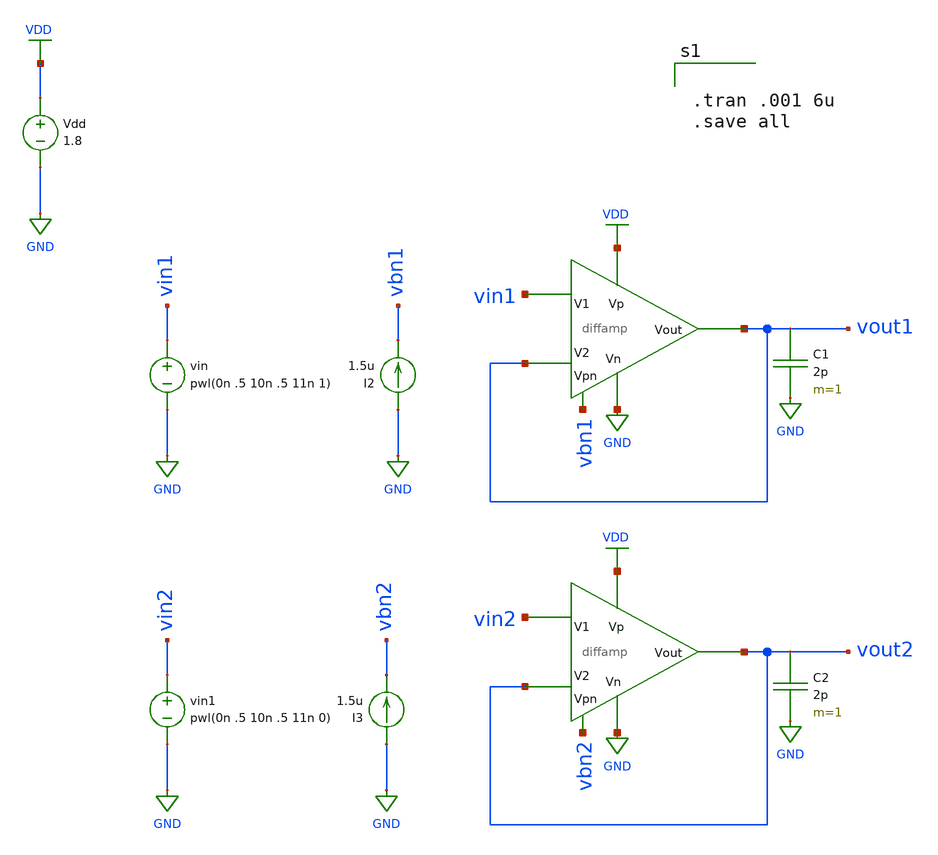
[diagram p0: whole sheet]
** sch_path: mini_proj_3/schematic/diff_2f.sch
**.subckt diff_2f
Vdd VDD GND 1.8
vin vin1 GND pwl(0n .5 10n .5 11n 1)
C1 vout1 GND 2p m=1
X1 vbn1 VDD GND vin1 vout1 vout1 diffamp
C2 vout2 GND 2p m=1
X2 vbn2 VDD GND vin2 vout2 vout2 diffamp
vin1 vin2 GND pwl(0n .5 10n .5 11n 0)
I2 GND vbn1 1.5u
I3 GND vbn2 1.5u
**** begin user architecture code

.option wnflag=1
.lib ~/skywater/skywater-pdk/libraries/sky130_fd_pr_ngspice/latest/models/sky130.lib.spice tt



.tran .001 6u
.save all


**** end user architecture code
**.ends
.GLOBAL VDD
.GLOBAL GND
.end
